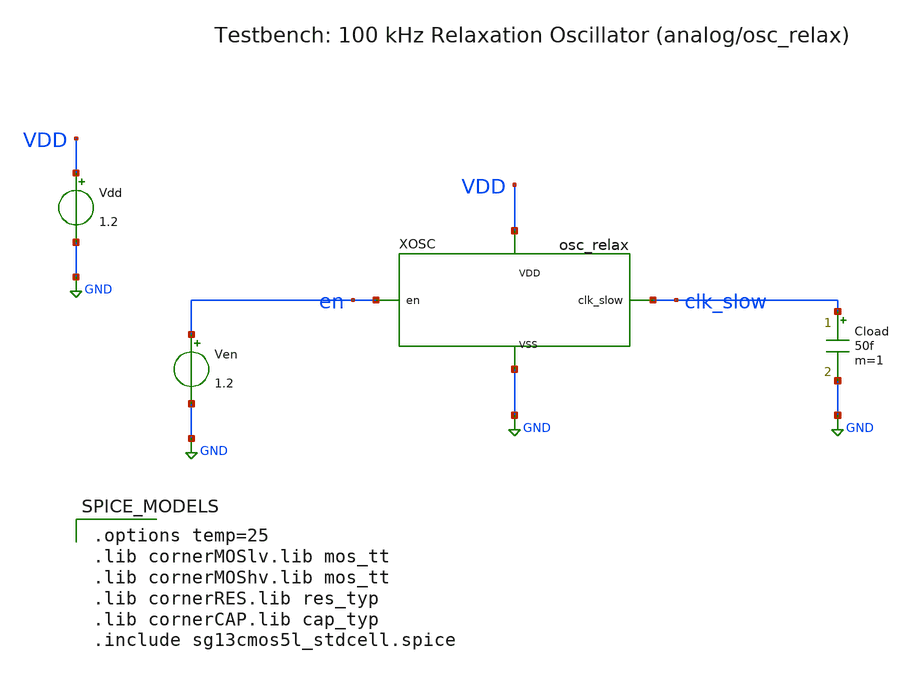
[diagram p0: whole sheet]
** sch_path: analog/osc_relax/tb_osc_relax.sch
**.subckt tb_osc_relax
XOSC VDD GND en clk_slow osc_relax
Vdd VDD GND 1.2
Ven en GND 1.2
Cload clk_slow GND 50f m=1
**** begin user architecture code

.options temp=25
.lib cornerMOSlv.lib mos_tt
.lib cornerMOShv.lib mos_tt
.lib cornerRES.lib res_typ
.lib cornerCAP.lib cap_typ
.include sg13cmos5l_stdcell.spice


**** end user architecture code
**.ends

* expanding   symbol:  osc_relax/osc_relax.sym # of pins=4
** sym_path: analog/osc_relax/osc_relax.sym
** sch_path: analog/osc_relax/osc_relax.sch
.subckt osc_relax VDD VSS en clk_slow
*.iopin VDD
*.iopin VSS
*.ipin en
*.opin clk_slow
XINV_EN enb en VDD VSS sg13cmos5l_inv_1
XBIAS VDD VSS en vpbias vnbias net9 bias
* noconn #net9
XMP_REF vth vpbias VDD VDD sg13_lv_pmos w=1.0u l=4.0u ng=1 m=1 mm_ok=1
XR_TH0 vth net1 VSS rppd w=0.5e-6 l=40.0e-6 m=1 b=9 mm_ok=1
XR_TH1 net1 net2 VSS rppd w=0.5e-6 l=40.0e-6 m=1 b=9 mm_ok=1
XR_TH2 net2 net3 VSS rppd w=0.5e-6 l=40.0e-6 m=1 b=9 mm_ok=1
XR_TH3 net3 VSS VSS rppd w=0.5e-6 l=40.0e-6 m=1 b=9 mm_ok=1
XMN_MIR vp_chg vnbias VSS VSS sg13_lv_nmos w=0.3u l=4.0u ng=1 m=1 mm_ok=1
XMP_CHG_IN vp_chg vp_chg VDD VDD sg13_lv_pmos w=0.5u l=4.0u ng=1 m=10 mm_ok=1
XMP_CHG_A vcap_a vp_chg VDD VDD sg13_lv_pmos w=0.5u l=4.0u ng=1 m=1 mm_ok=1
XMN_DIS_A vcap_a dis_a VSS VSS sg13_hv_nmos w=0.5u l=0.5u ng=1 m=1 mm_ok=1
XC_A vcap_a VSS cap_cmomf w=20.6e-6 l=20.6e-6 mmin=1 mmax=4 subblock=0 rfmodel=0 subscale=1 m=1
+ mm_ok=1
XCOMP_A VDD VSS en vpbias vcap_a vth cmp_a comp
XMP_CHG_B vcap_b vp_chg VDD VDD sg13_lv_pmos w=0.5u l=4.0u ng=1 m=1 mm_ok=1
XMN_DIS_B vcap_b dis_b VSS VSS sg13_hv_nmos w=0.5u l=0.5u ng=1 m=1 mm_ok=1
XC_B vcap_b VSS cap_cmomf w=20.6e-6 l=20.6e-6 mmin=1 mmax=4 subblock=0 rfmodel=0 subscale=1 m=1
+ mm_ok=1
XCOMP_B VDD VSS en vpbias vcap_b vth cmp_b comp
XSR_Q q cmp_b qb VDD VSS sg13cmos5l_nor2_1
XSR_QB qb cmp_a q VDD VSS sg13cmos5l_nor2_1
XMN_INIT qb enb VSS VSS sg13_lv_nmos w=0.5u l=0.5u ng=1 m=1 mm_ok=1
XDIS_N_A net4 q enb VDD VSS sg13cmos5l_nor2_1
XDIS_I_A dis_a net4 VDD VSS sg13cmos5l_inv_1
XDIS_N_B net5 qb enb VDD VSS sg13cmos5l_nor2_1
XDIS_I_B dis_b net5 VDD VSS sg13cmos5l_inv_1
XBOTH_NAND net6 cmp_a cmp_b VDD VSS sg13cmos5l_nand2_2
XBOTH_INV net7 net6 VDD VSS sg13cmos5l_inv_1
XMN_UNSTICK vcap_a net7 VSS VSS sg13_hv_nmos w=0.5u l=0.5u ng=1 m=1 mm_ok=1
XOUT_NOR net8 qb enb VDD VSS sg13cmos5l_nor2_1
XOUT_BUF clk_slow net8 VDD VSS sg13cmos5l_buf_2
.ends


* expanding   symbol:  bias/bias.sym # of pins=6
** sym_path: analog/bias/bias.sym
** sch_path: analog/bias/bias.sch
.subckt bias VDD VSS en vpbias vnbias ibias_out
*.iopin VDD
*.iopin VSS
*.ipin en
*.opin vpbias
*.opin vnbias
*.opin ibias_out
XMEN_P enb en VDD VDD sg13_lv_pmos w=0.5u l=0.5u ng=1 m=1 mm_ok=1
XMEN_N enb en VSS VSS sg13_lv_nmos w=0.25u l=0.5u ng=1 m=1 mm_ok=1
XMSU_EN net1 enb VDD VDD sg13_lv_pmos w=0.3u l=1.0u ng=1 m=1 mm_ok=1
XMSU_P1 net2 VSS net1 VDD sg13_lv_pmos w=0.15u l=10u ng=1 m=1 mm_ok=1
XMSU_P2 net3 VSS net2 VDD sg13_lv_pmos w=0.15u l=10u ng=1 m=1 mm_ok=1
XMSU_N net3 vnbias VSS VSS sg13_lv_nmos w=4.0u l=0.5u ng=1 m=1 mm_ok=1
XMSU_INJ vpbias net3 VSS VSS sg13_lv_nmos w=0.5u l=1.0u ng=1 m=1 mm_ok=1
XMP1 vnbias vpbias VDD VDD sg13_lv_pmos w=1.0u l=4.0u ng=1 m=1 mm_ok=1
XMN1 vnbias vnbias VSS VSS sg13_lv_nmos w=0.3u l=4.0u ng=1 m=1 mm_ok=1
XMP2 vpbias vpbias VDD VDD sg13_lv_pmos w=1.0u l=4.0u ng=1 m=1 mm_ok=1
XMN2 vpbias vnbias net4 VSS sg13_lv_nmos w=0.3u l=4.0u ng=1 m=4 mm_ok=1
XR_BIAS net4 VSS VSS rppd w=0.5e-6 l=20.0e-6 m=1 b=19 mm_ok=1
XMP_OFF vpbias en VDD VDD sg13_lv_pmos w=1.0u l=0.5u ng=1 m=1 mm_ok=1
XMN_OFF vnbias enb VSS VSS sg13_lv_nmos w=1.0u l=0.5u ng=1 m=1 mm_ok=1
XMP_OUT ibias_out vpbias VDD VDD sg13_lv_pmos w=1.0u l=4.0u ng=1 m=1 mm_ok=1
.ends


* expanding   symbol:  osc_relax/comp.sym # of pins=7
** sym_path: analog/osc_relax/comp.sym
** sch_path: analog/osc_relax/comp.sch
.subckt comp VDD VSS en vpbias inp inn out
*.iopin VDD
*.iopin VSS
*.ipin en
*.ipin vpbias
*.ipin inp
*.ipin inn
*.opin out
XMP_TAIL net1 vpbias VDD VDD sg13_lv_pmos w=1.0u l=4.0u ng=1 m=1 mm_ok=1
XMP_INP net2 inp net1 VDD sg13_lv_pmos w=2.0u l=1.0u ng=1 m=2 mm_ok=1
XMP_INN net3 inn net1 VDD sg13_lv_pmos w=2.0u l=1.0u ng=1 m=2 mm_ok=1
XMN_L1 net2 net2 VSS VSS sg13_lv_nmos w=0.5u l=2.0u ng=1 m=1 mm_ok=1
XMN_L2 net3 net2 VSS VSS sg13_lv_nmos w=0.5u l=2.0u ng=1 m=1 mm_ok=1
XMP_G2 net4 vpbias VDD VDD sg13_lv_pmos w=1.0u l=4.0u ng=1 m=1 mm_ok=1
XMN_G2 net4 net3 VSS VSS sg13_lv_nmos w=1.0u l=1.0u ng=1 m=1 mm_ok=1
XMP_OFF net4 en VDD VDD sg13_lv_pmos w=0.5u l=0.5u ng=1 m=1 mm_ok=1
XINV_OUT out net4 VDD VSS sg13cmos5l_inv_1
.ends

.GLOBAL GND
.end
